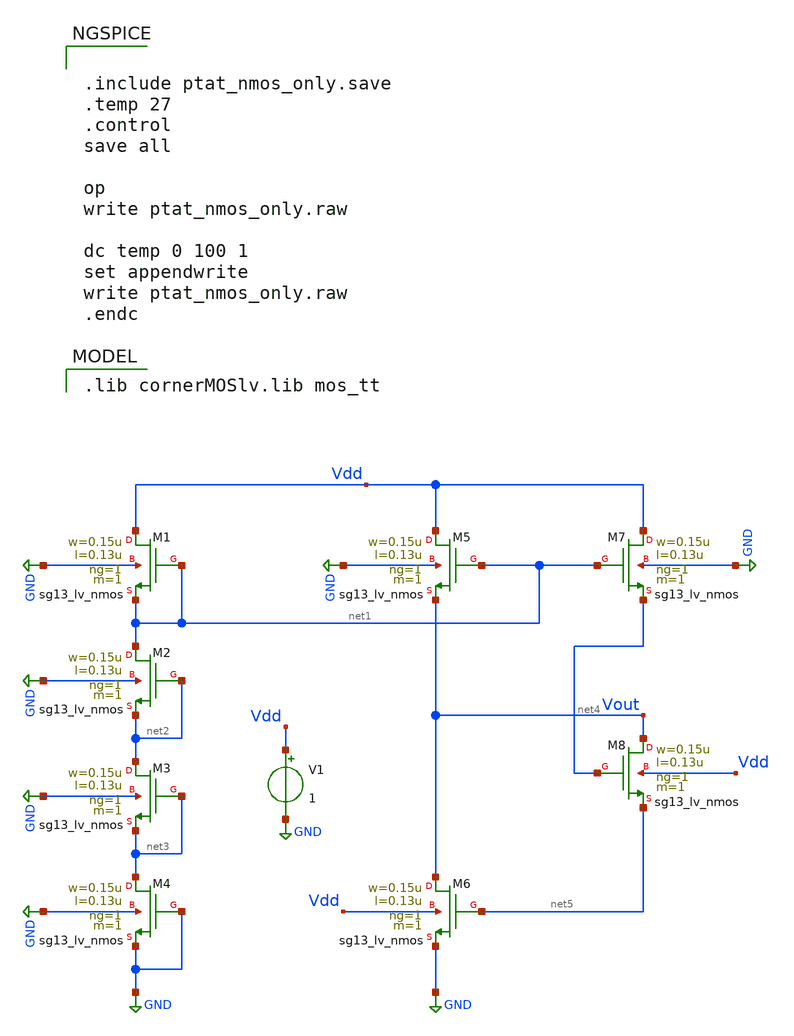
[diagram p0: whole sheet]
** sch_path: TempSensor/design_data/xschem/ptat_nmos_only.sch
**.subckt ptat_nmos_only
XM1 Vdd net1 net1 GND sg13_lv_nmos w=0.15u l=0.13u ng=1 m=1 mm_ok=1
XM2 net1 net2 net2 GND sg13_lv_nmos w=0.15u l=0.13u ng=1 m=1 mm_ok=1
XM3 net2 net3 net3 GND sg13_lv_nmos w=0.15u l=0.13u ng=1 m=1 mm_ok=1
XM4 net3 GND GND GND sg13_lv_nmos w=0.15u l=0.13u ng=1 m=1 mm_ok=1
XM5 Vdd net1 Vout GND sg13_lv_nmos w=0.15u l=0.13u ng=1 m=1 mm_ok=1
XM6 Vout net5 GND Vdd sg13_lv_nmos w=0.15u l=0.13u ng=1 m=1 mm_ok=1
XM7 Vdd net1 net4 GND sg13_lv_nmos w=0.15u l=0.13u ng=1 m=1 mm_ok=1
XM8 Vout net4 net5 Vdd sg13_lv_nmos w=0.15u l=0.13u ng=1 m=1 mm_ok=1
V1 Vdd GND 1
**** begin user architecture code


.include ptat_nmos_only.save
.temp 27
.control
save all

op
write ptat_nmos_only.raw

dc temp 0 100 1
set appendwrite
write ptat_nmos_only.raw
.endc


 .lib cornerMOSlv.lib mos_tt

**** end user architecture code
**.ends
.GLOBAL GND
.end
